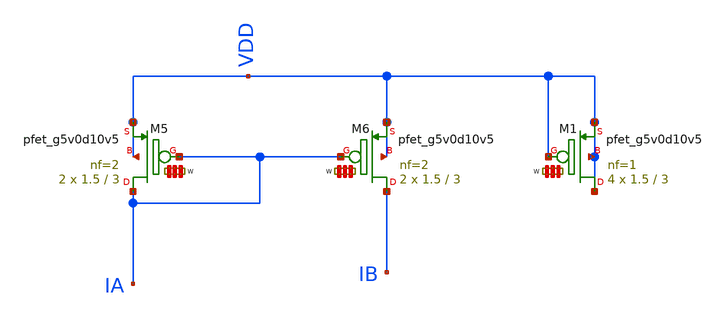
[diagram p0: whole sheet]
** sch_path: Learning/single_ended_amplifiers/Design_transcondutance_cell_sky130_5V/layout_example/pmos_current_mirror_old/pmos_current_mirror.sch
**.subckt pmos_current_mirror
XM5 IA IA VDD VDD sky130_fd_pr__pfet_g5v0d10v5 L=3 W='1.5 * 2 ' nf=2 ad='int((2 + 1)/2) * 1.5 * 0.29'
+ as='int((2 + 2)/2) * 1.5 * 0.29' pd='2*int((2 + 1)/2) * (1.5 + 0.29)' ps='2*int((2 + 2)/2) * (1.5 + 0.29)'
+ nrd='0.29 / 1.5 / 2 ' nrs='0.29 / 1.5 / 2 ' sa=0 sb=0 sd=0 mult=2 m=2
XM6 IB IA VDD VDD sky130_fd_pr__pfet_g5v0d10v5 L=3 W='1.5 * 2 ' nf=2 ad='int((2 + 1)/2) * 1.5 * 0.29'
+ as='int((2 + 2)/2) * 1.5 * 0.29' pd='2*int((2 + 1)/2) * (1.5 + 0.29)' ps='2*int((2 + 2)/2) * (1.5 + 0.29)'
+ nrd='0.29 / 1.5 / 2 ' nrs='0.29 / 1.5 / 2 ' sa=0 sb=0 sd=0 mult=2 m=2
XM1 VDD VDD VDD VDD sky130_fd_pr__pfet_g5v0d10v5 L=3 W='1.5 * 1 ' nf=1 ad='int((1 + 1)/2) * 1.5 * 0.29'
+ as='int((1 + 2)/2) * 1.5 * 0.29' pd='2*int((1 + 1)/2) * (1.5 + 0.29)' ps='2*int((1 + 2)/2) * (1.5 + 0.29)'
+ nrd='0.29 / 1.5 / 1 ' nrs='0.29 / 1.5 / 1 ' sa=0 sb=0 sd=0 mult=4 m=4
**.ends
.end
